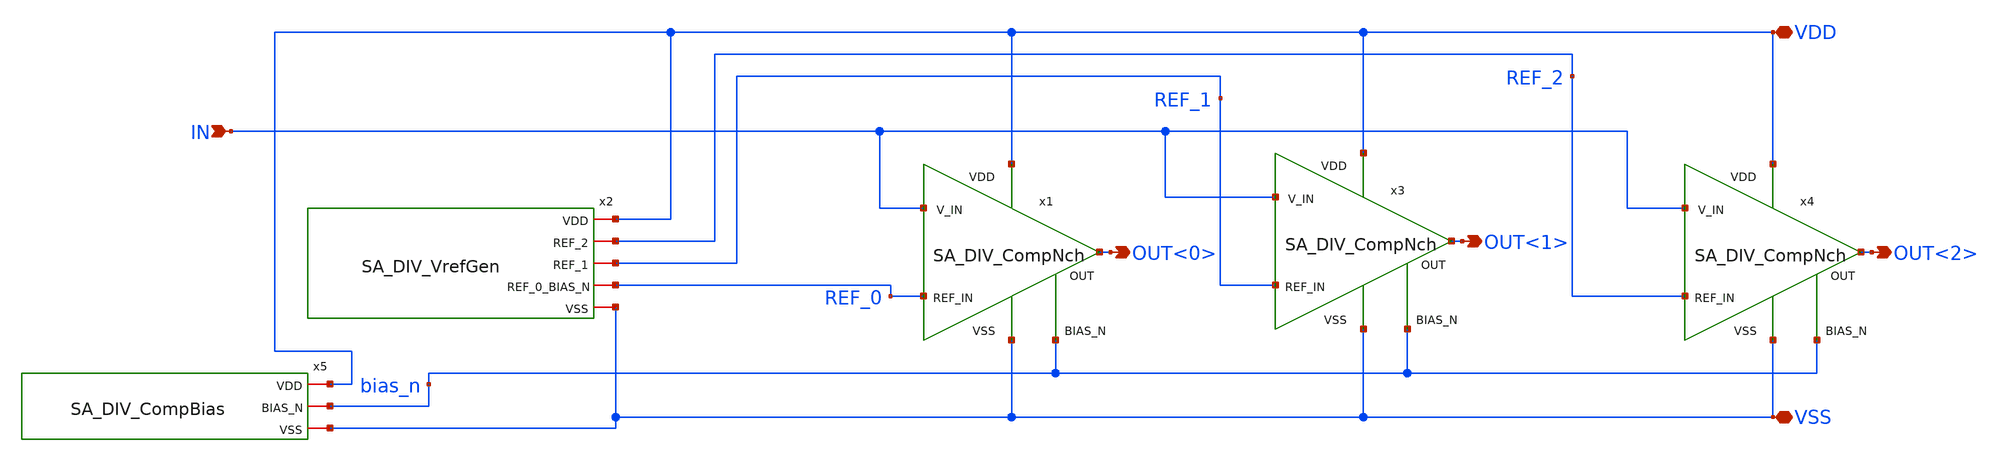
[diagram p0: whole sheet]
** sch_path: design/.design_bk/xschem/VCO/SA_DIV_ADC.sch
**.subckt SA_DIV_ADC IN OUT<0> OUT<1> OUT<2> VDD VSS
*.ipin IN
*.opin OUT<0>
*.opin OUT<1>
*.opin OUT<2>
*.iopin VDD
*.iopin VSS
x1 VDD OUT<0> REF_0 IN bias_n VSS SA_DIV_CompNch
x2 VDD REF_2 REF_1 REF_0 VSS SA_DIV_VrefGen
x3 VDD OUT<1> REF_1 IN bias_n VSS SA_DIV_CompNch
x4 VDD OUT<2> REF_2 IN bias_n VSS SA_DIV_CompNch
x5 VDD bias_n VSS SA_DIV_CompBias
**.ends
.end
